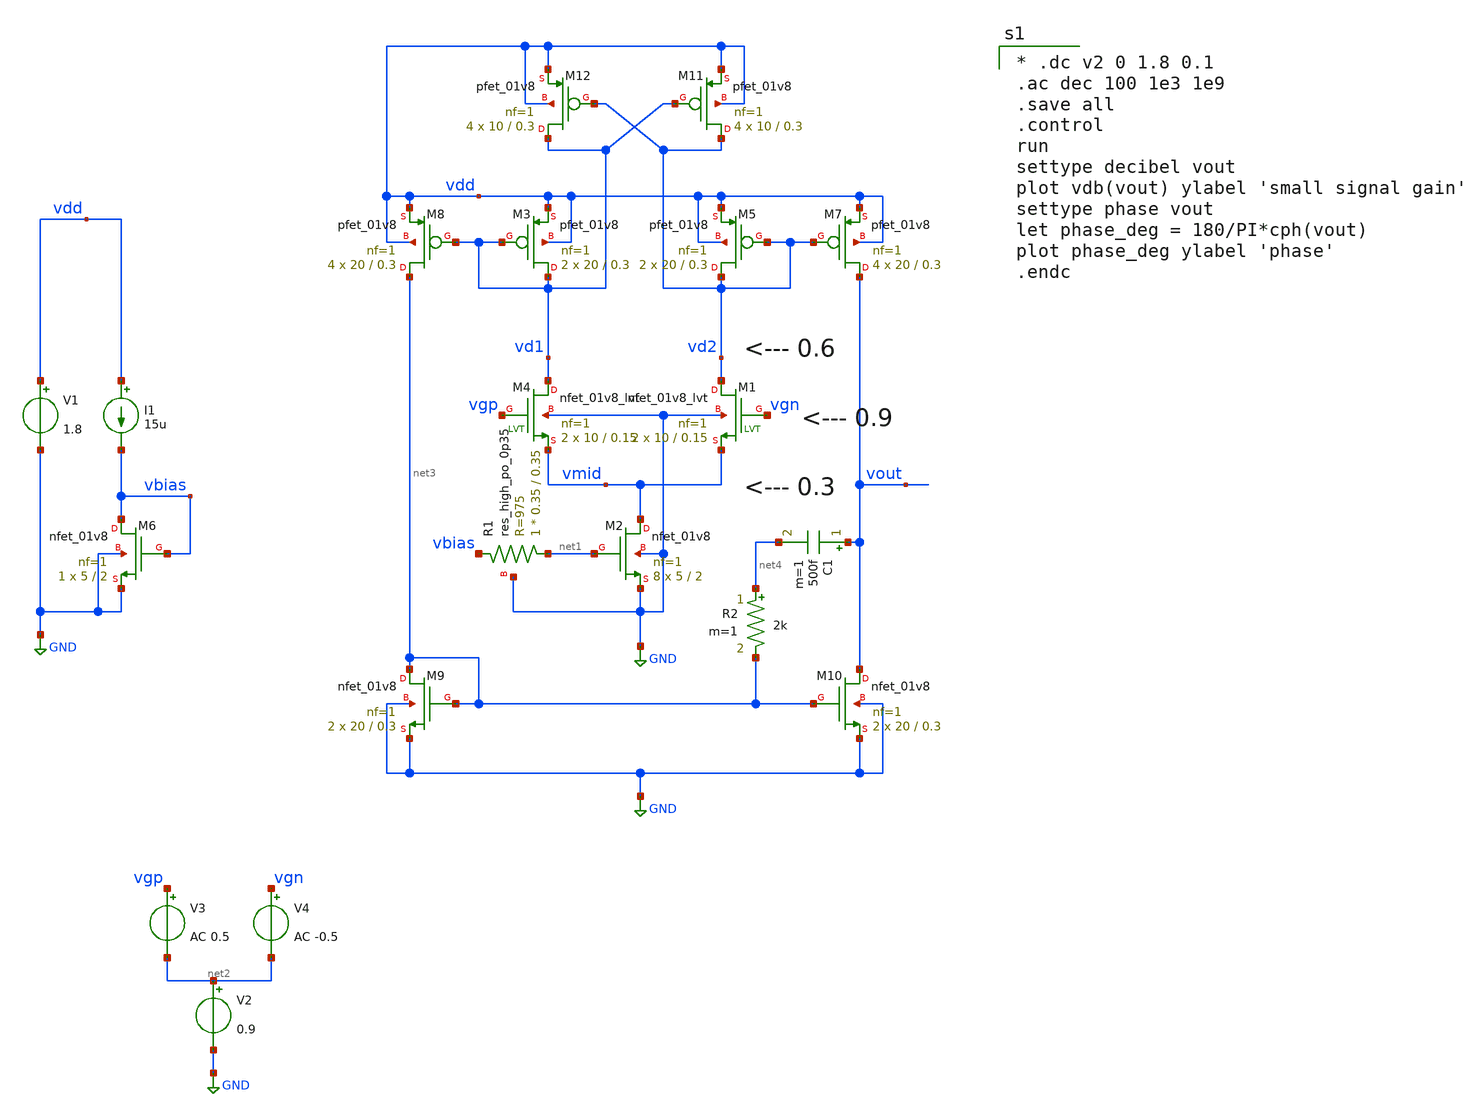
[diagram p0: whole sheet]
** sch_path: xschem/i_type_ota.sch
**.subckt i_type_ota
XM2 vmid net1 GND GND sky130_fd_pr__nfet_01v8 L=2 W=5 nf=1 ad='int((nf+1)/2) * W/nf * 0.29' as='int((nf+2)/2) * W/nf * 0.29'
+ pd='2*int((nf+1)/2) * (W/nf + 0.29)' ps='2*int((nf+2)/2) * (W/nf + 0.29)' nrd='0.29 / W' nrs='0.29 / W'
+ sa=0 sb=0 sd=0 mult=8 m=8
XM6 vbias vbias GND GND sky130_fd_pr__nfet_01v8 L=2 W=5 nf=1 ad='int((nf+1)/2) * W/nf * 0.29' as='int((nf+2)/2) * W/nf * 0.29'
+ pd='2*int((nf+1)/2) * (W/nf + 0.29)' ps='2*int((nf+2)/2) * (W/nf + 0.29)' nrd='0.29 / W' nrs='0.29 / W'
+ sa=0 sb=0 sd=0 mult=1 m=1
I1 vdd vbias 15u
XR1 net1 vbias GND sky130_fd_pr__res_high_po_0p35 L=0.35 mult=1 m=1
V1 vdd GND 1.8
V2 net2 GND 0.9
V3 vgp net2 AC 0.5
V4 vgn net2 AC -0.5
XM4 vd1 vgp vmid GND sky130_fd_pr__nfet_01v8_lvt L=0.15 W=10 nf=1 ad='int((nf+1)/2) * W/nf * 0.29' as='int((nf+2)/2) * W/nf * 0.29'
+ pd='2*int((nf+1)/2) * (W/nf + 0.29)' ps='2*int((nf+2)/2) * (W/nf + 0.29)' nrd='0.29 / W' nrs='0.29 / W'
+ sa=0 sb=0 sd=0 mult=2 m=2
XM1 vd2 vgn vmid GND sky130_fd_pr__nfet_01v8_lvt L=0.15 W=10 nf=1 ad='int((nf+1)/2) * W/nf * 0.29' as='int((nf+2)/2) * W/nf * 0.29'
+ pd='2*int((nf+1)/2) * (W/nf + 0.29)' ps='2*int((nf+2)/2) * (W/nf + 0.29)' nrd='0.29 / W' nrs='0.29 / W'
+ sa=0 sb=0 sd=0 mult=2 m=2
XM3 vd1 vd1 vdd vdd sky130_fd_pr__pfet_01v8 L=0.3 W=20 nf=1 ad='int((nf+1)/2) * W/nf * 0.29' as='int((nf+2)/2) * W/nf * 0.29'
+ pd='2*int((nf+1)/2) * (W/nf + 0.29)' ps='2*int((nf+2)/2) * (W/nf + 0.29)' nrd='0.29 / W' nrs='0.29 / W'
+ sa=0 sb=0 sd=0 mult=2 m=2
XM5 vd2 vd2 vdd vdd sky130_fd_pr__pfet_01v8 L=0.3 W=20 nf=1 ad='int((nf+1)/2) * W/nf * 0.29' as='int((nf+2)/2) * W/nf * 0.29'
+ pd='2*int((nf+1)/2) * (W/nf + 0.29)' ps='2*int((nf+2)/2) * (W/nf + 0.29)' nrd='0.29 / W' nrs='0.29 / W'
+ sa=0 sb=0 sd=0 mult=2 m=2
XM7 vout vd2 vdd vdd sky130_fd_pr__pfet_01v8 L=0.3 W=20 nf=1 ad='int((nf+1)/2) * W/nf * 0.29' as='int((nf+2)/2) * W/nf * 0.29'
+ pd='2*int((nf+1)/2) * (W/nf + 0.29)' ps='2*int((nf+2)/2) * (W/nf + 0.29)' nrd='0.29 / W' nrs='0.29 / W'
+ sa=0 sb=0 sd=0 mult=4 m=4
XM8 net3 vd1 vdd vdd sky130_fd_pr__pfet_01v8 L=0.3 W=20 nf=1 ad='int((nf+1)/2) * W/nf * 0.29' as='int((nf+2)/2) * W/nf * 0.29'
+ pd='2*int((nf+1)/2) * (W/nf + 0.29)' ps='2*int((nf+2)/2) * (W/nf + 0.29)' nrd='0.29 / W' nrs='0.29 / W'
+ sa=0 sb=0 sd=0 mult=4 m=4
XM9 net3 net3 GND GND sky130_fd_pr__nfet_01v8 L=0.3 W=20 nf=1 ad='int((nf+1)/2) * W/nf * 0.29' as='int((nf+2)/2) * W/nf * 0.29'
+ pd='2*int((nf+1)/2) * (W/nf + 0.29)' ps='2*int((nf+2)/2) * (W/nf + 0.29)' nrd='0.29 / W' nrs='0.29 / W'
+ sa=0 sb=0 sd=0 mult=2 m=2
XM10 vout net3 GND GND sky130_fd_pr__nfet_01v8 L=0.3 W=20 nf=1 ad='int((nf+1)/2) * W/nf * 0.29' as='int((nf+2)/2) * W/nf * 0.29'
+ pd='2*int((nf+1)/2) * (W/nf + 0.29)' ps='2*int((nf+2)/2) * (W/nf + 0.29)' nrd='0.29 / W' nrs='0.29 / W'
+ sa=0 sb=0 sd=0 mult=2 m=2
XM11 vd2 vd1 vdd vdd sky130_fd_pr__pfet_01v8 L=0.3 W=10 nf=1 ad='int((nf+1)/2) * W/nf * 0.29' as='int((nf+2)/2) * W/nf * 0.29'
+ pd='2*int((nf+1)/2) * (W/nf + 0.29)' ps='2*int((nf+2)/2) * (W/nf + 0.29)' nrd='0.29 / W' nrs='0.29 / W'
+ sa=0 sb=0 sd=0 mult=4 m=4
XM12 vd1 vd2 vdd vdd sky130_fd_pr__pfet_01v8 L=0.3 W=10 nf=1 ad='int((nf+1)/2) * W/nf * 0.29' as='int((nf+2)/2) * W/nf * 0.29'
+ pd='2*int((nf+1)/2) * (W/nf + 0.29)' ps='2*int((nf+2)/2) * (W/nf + 0.29)' nrd='0.29 / W' nrs='0.29 / W'
+ sa=0 sb=0 sd=0 mult=4 m=4
C1 vout net4 500f m=1
R2 net4 net3 2k m=1
**** begin user architecture code
.lib $::SKYWATER_MODELS/sky130.lib.spice tt
.include $::PDKPATH/libs.ref/sky130_fd_sc_hs/spice/sky130_fd_sc_hs.spice


* .dc v2 0 1.8 0.1
.ac dec 100 1e3 1e9
.save all
.control
run
settype decibel vout
plot vdb(vout) ylabel 'small signal gain'
settype phase vout
let phase_deg = 180/PI*cph(vout)
plot phase_deg ylabel 'phase'
.endc


**** end user architecture code
**.ends
.GLOBAL GND
.end
